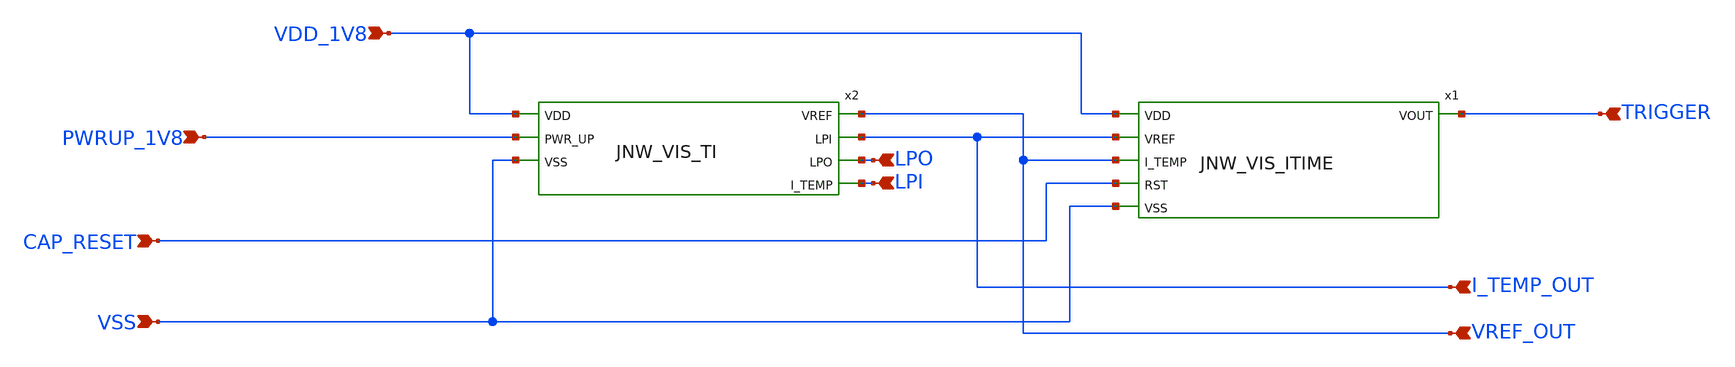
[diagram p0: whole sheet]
** sch_path: design/JNW_GR02_SKY130A/JNW_GR02.sch
**.subckt JNW_GR02 VDD_1V8 VSS PWRUP_1V8 TRIGGER CAP_RESET I_TEMP_OUT LPI LPO VREF_OUT
*.ipin VDD_1V8
*.ipin VSS
*.ipin PWRUP_1V8
*.ipin TRIGGER
*.ipin CAP_RESET
*.ipin I_TEMP_OUT
*.ipin LPI
*.ipin LPO
*.ipin VREF_OUT
x1 VDD_1V8 I_TEMP_OUT TRIGGER VREF_OUT CAP_RESET VSS JNW_VIS_ITIME
x2 VDD_1V8 VREF_OUT I_TEMP_OUT LPO LPI PWRUP_1V8 VSS JNW_VIS_TI
**.ends
.end
